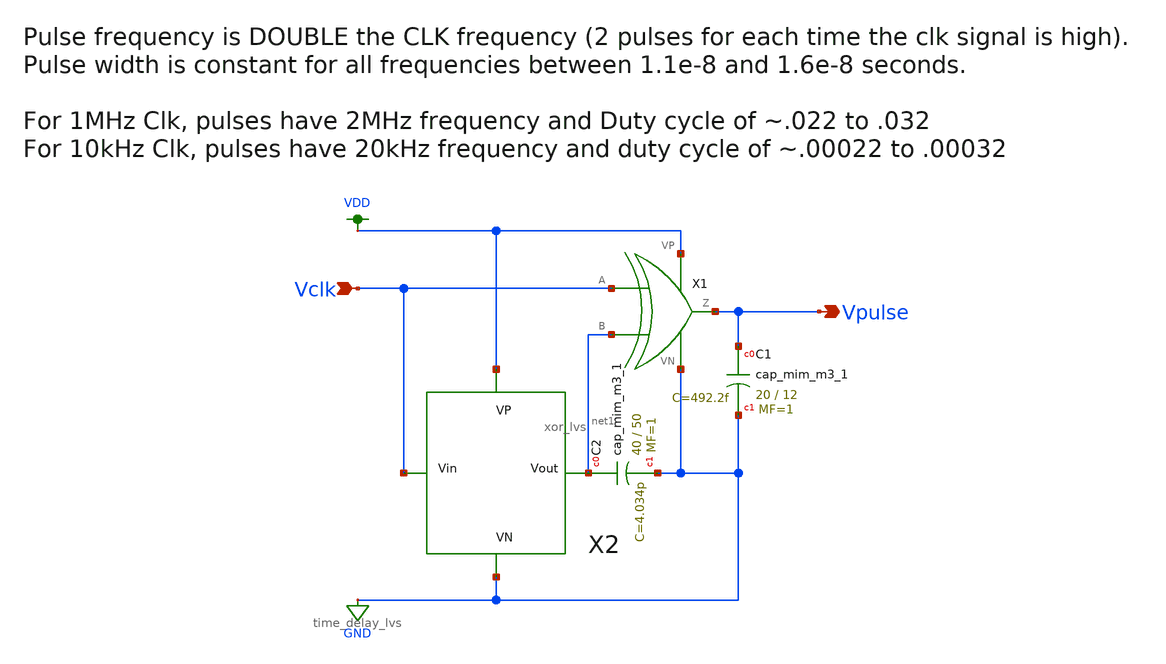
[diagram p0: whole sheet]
** sch_path: schematics/pulse_generator_lvs.sch
**.subckt pulse_generator_lvs Vpulse Vclk
*.opin Vpulse
*.ipin Vclk
XC1 Vpulse GND sky130_fd_pr__cap_mim_m3_1 W=20 L=12 MF=1 m=1
XC2 net1 GND sky130_fd_pr__cap_mim_m3_1 W=40 L=50 MF=1 m=1
X2 Vclk VDD GND net1 time_delay_lvs
X1 Vclk net1 VDD GND Vpulse xor_lvs
**.ends
.GLOBAL VDD
.GLOBAL GND
.end
